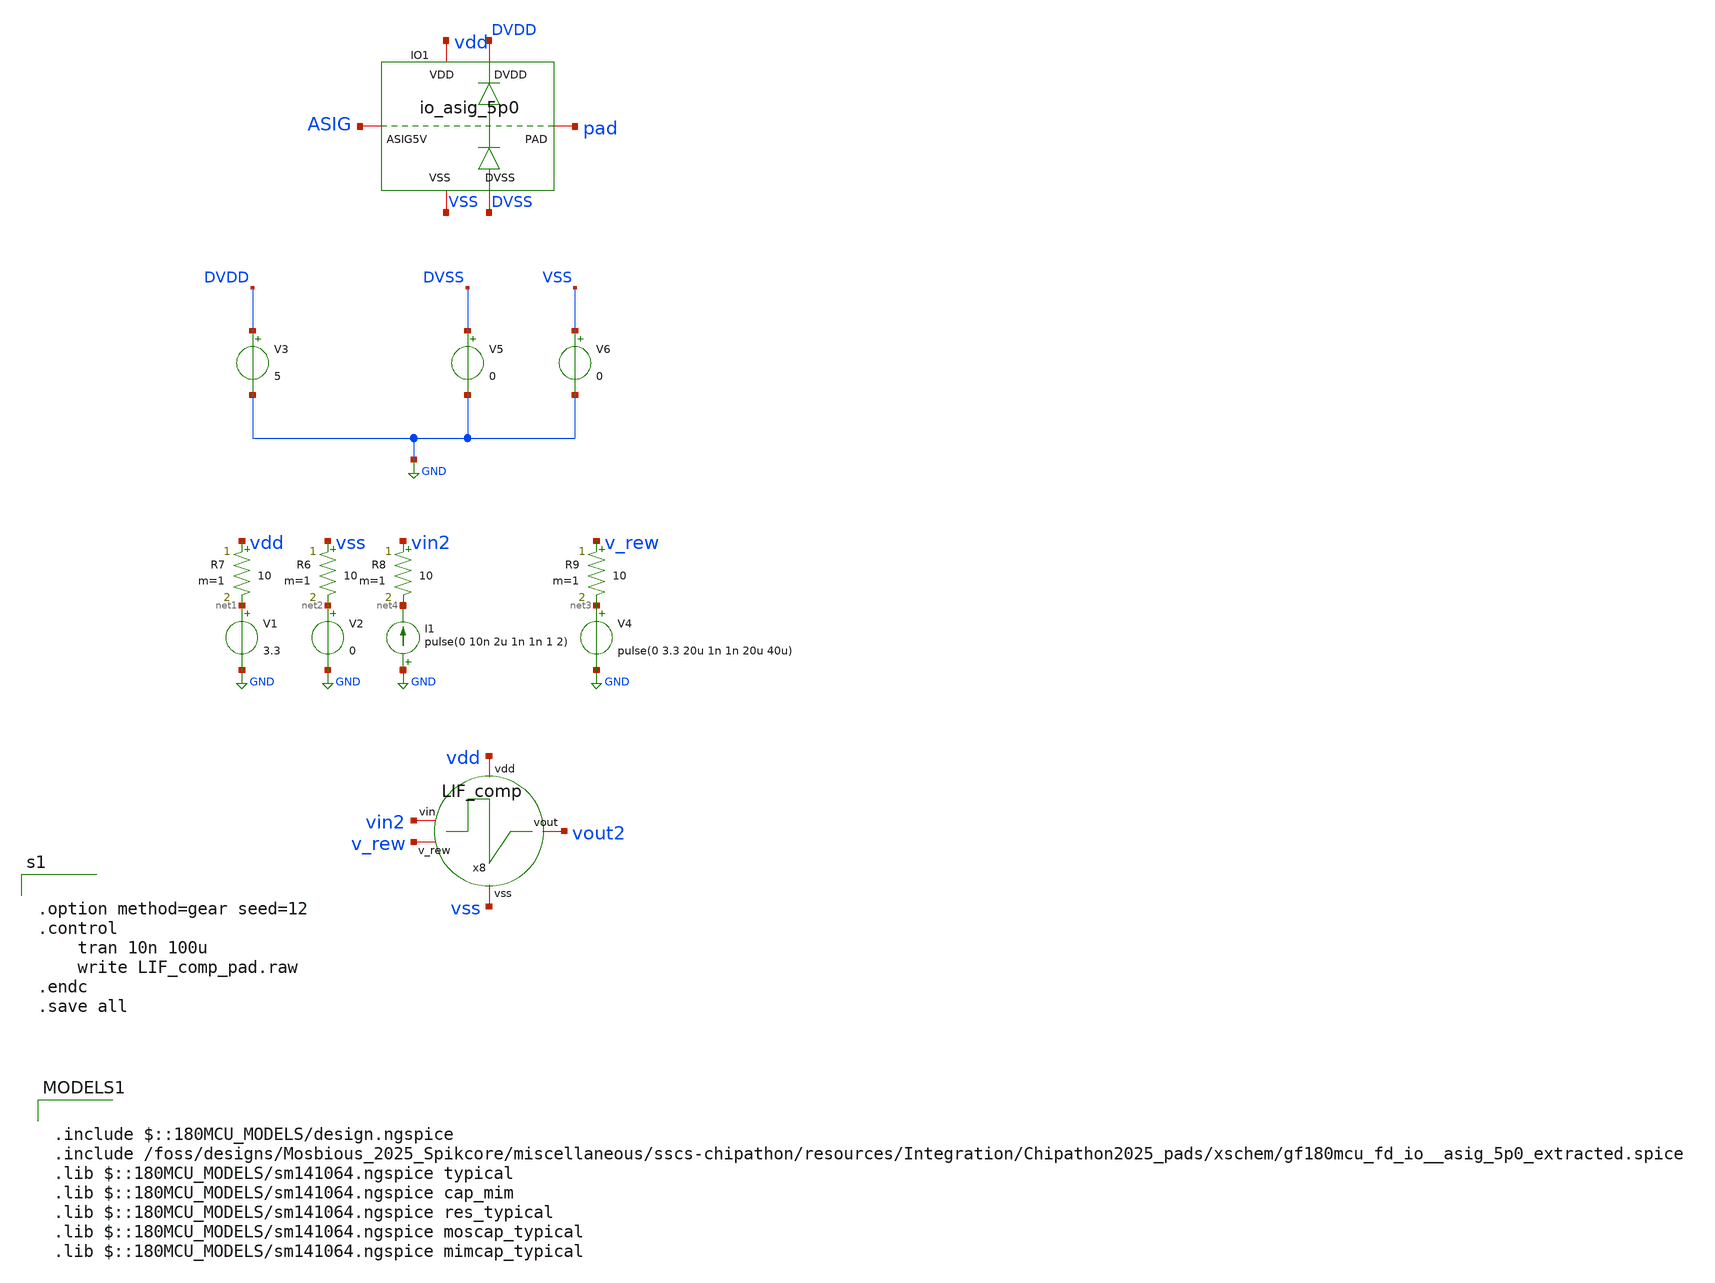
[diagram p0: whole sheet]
** sch_path: designs/libs/tb_core_analogs_pads/tb_LIF_comp/LIF_comp.sch
**.subckt LIF_comp
V1 net1 GND 3.3
V2 net2 GND 0
V4 net3 GND pulse(0 3.3 20u 1n 1n 20u 40u)
x8 vdd vss vin2 v_rew vout2 LIF_comp
I1 GND net4 pulse(0 10n 2u 1n 1n 1 2)
R6 vss net2 10 m=1
R7 vdd net1 10 m=1
R8 vin2 net4 10 m=1
R9 v_rew net3 10 m=1
V3 DVDD GND 5
V5 DVSS GND 0
V6 VSS GND 0
XIO1 DVSS DVDD VSS vdd pad ASIG gf180mcu_fd_io__asig_5p0_extracted
**** begin user architecture code


.option method=gear seed=12
.control
    tran 10n 100u
    write LIF_comp_pad.raw
.endc
.save all



.include $::180MCU_MODELS/design.ngspice
.include /foss/designs/Mosbious_2025_Spikcore/miscellaneous/sscs-chipathon/resources/Integration/Chipathon2025_pads/xschem/gf180mcu_fd_io__asig_5p0_extracted.spice
.lib $::180MCU_MODELS/sm141064.ngspice typical
.lib $::180MCU_MODELS/sm141064.ngspice cap_mim
.lib $::180MCU_MODELS/sm141064.ngspice res_typical
.lib $::180MCU_MODELS/sm141064.ngspice moscap_typical
.lib $::180MCU_MODELS/sm141064.ngspice mimcap_typical

**** end user architecture code
**.ends
.GLOBAL GND
.end
